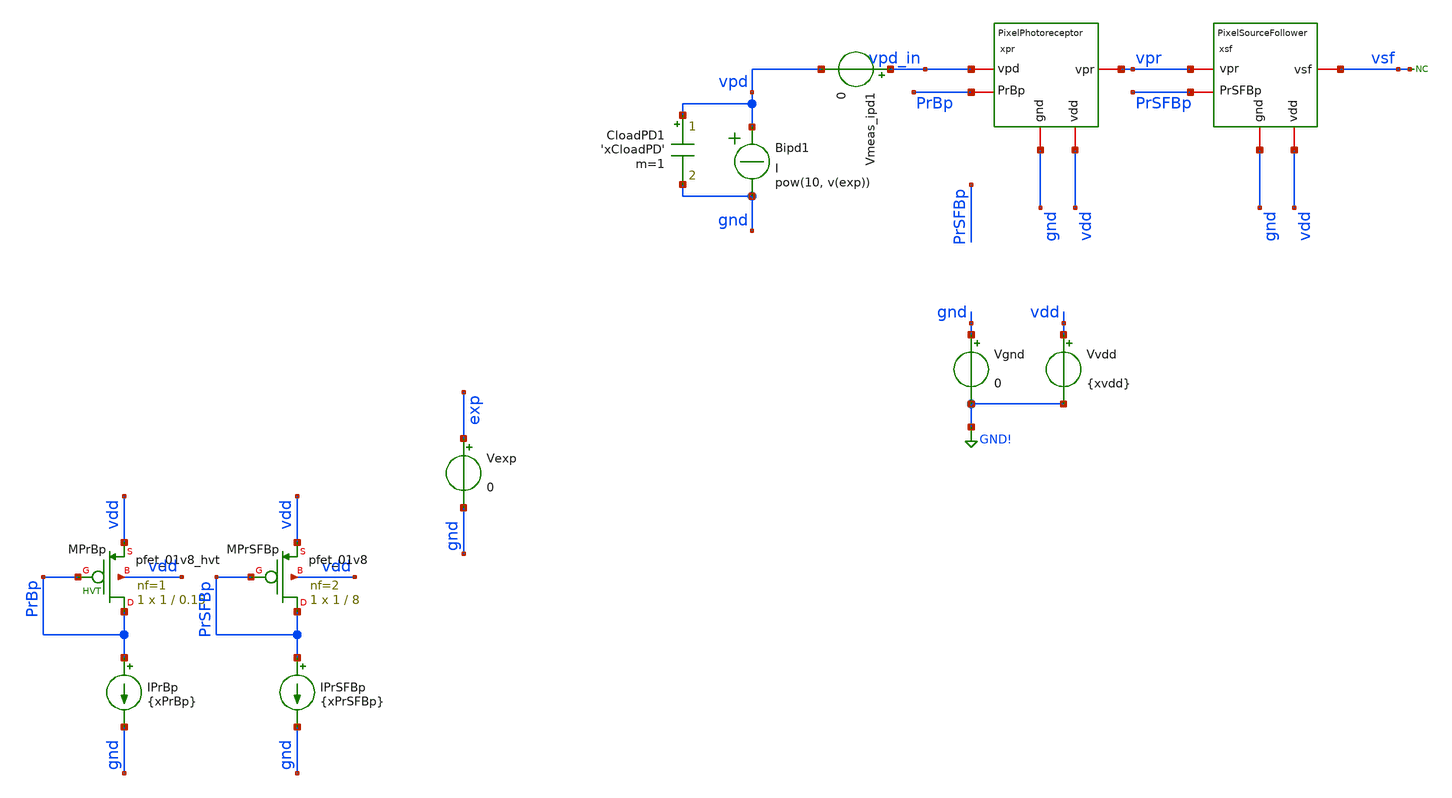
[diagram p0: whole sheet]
** sch_path: analog/klayout/production/final_merge_20260923/testbenches/cace/analog/xschem/tb_PixelPhotoreceptor_dc.sch
**.subckt tb_PixelPhotoreceptor_dc
IPrBp PrBp gnd {xPrBp}
XMPrBp PrBp PrBp vdd vdd sky130_fd_pr__pfet_01v8_hvt L=0.15 W=1 nf=1 ad='int((1 + 1)/2) * 1 / 1 * 0.29'
+ as='int((1 + 2)/2) * 1 / 1 * 0.29' pd='2*int((1 + 1)/2) * (1 / 1 + 0.29)' ps='2*int((1 + 2)/2) * (1 / 1 + 0.29)'
+ nrd='0.29 / 1 ' nrs='0.29 / 1 ' sa=0 sb=0 sd=0 mult=1 m=1
IPrSFBp PrSFBp gnd {xPrSFBp}
XMPrSFBp PrSFBp PrSFBp vdd vdd sky130_fd_pr__pfet_01v8 L=8 W=1 nf=2 ad='int((2 + 1)/2) * 1 / 2 * 0.29'
+ as='int((2 + 2)/2) * 1 / 2 * 0.29' pd='2*int((2 + 1)/2) * (1 / 2 + 0.29)' ps='2*int((2 + 2)/2) * (1 / 2 + 0.29)'
+ nrd='0.29 / 1 ' nrs='0.29 / 1 ' sa=0 sb=0 sd=0 mult=1 m=1
xpr vdd PrBp gnd vpd_in vpr PixelPhotoreceptor
xsf vdd PrSFBp gnd vpr vsf PixelSourceFollower
Bipd1 vpd gnd I = pow(10, v(exp))
CloadPD1 vpd gnd 'xCloadPD' m=1
Vmeas_ipd1 vpd_in vpd 0
* noconn vsf
Vexp exp gnd 0
Vgnd gnd GND! 0
Vvdd vdd GND! {xvdd}
**** begin user architecture code

** opencircuitdesign pdks install
.lib $::SKYWATER_MODELS/sky130.lib.spice tt



.include /home/rpgraca/research/projects/telluride/2025/nic_eventcam/nic2025_openDVS/analog/xschem/dvs_readout_ctrl.spice

** Convergence options for nA-range weak-inversion pixel circuit
** gmin=1e-15: at 1V node this is 1fA shunt, negligible vs nA signals
** method=gear: damps numerical ringing on stiff circuits (fast digital + slow analog)
** trtol=1: conservative timestep control prevents overshoot at edges
.option gmin=1e-16 abstol=1e-15 vntol=1e-9 reltol=1e-4 chgtol=1e-16
.option method=gear maxord=2 trtol=1
.option itl1=500 itl2=200 itl4=50
.option gminsteps=200 srcsteps=200
.option ramptime=100n

.dc Vexp -14 -7 0.2


.param xvdd = 1.8
*.param xipd = 1e-9
.param xPrBp = 10n
.param xPrSFBp = 100p
.param xCloadPD = 30f

** xipd swept via Vexp: Iipd uses behavioral expression

*Small Iphoto testing

.save all



**** end user architecture code
**.ends

* expanding   symbol:  PixelPhotoreceptor.sym # of pins=5
** sym_path: analog/xschem/PixelPhotoreceptor.sym
** sch_path: analog/xschem/PixelPhotoreceptor.sch
.subckt PixelPhotoreceptor vdd PrBp gnd vpd vpr
*.iopin PrBp
*.iopin vdd
*.iopin vpd
*.iopin gnd
*.iopin vpr
XMpd vdd vpr vpd gnd sky130_fd_pr__nfet_01v8 L=0.3 W=0.42 nf=1 ad='int((1 + 1)/2) * 0.42 / 1 * 0.29'
+ as='int((1 + 2)/2) * 0.42 / 1 * 0.29' pd='2*int((1 + 1)/2) * (0.42 / 1 + 0.29)' ps='2*int((1 + 2)/2) * (0.42 / 1 + 0.29)'
+ nrd='0.29 / 0.42 ' nrs='0.29 / 0.42 ' sa=0 sb=0 sd=0 mult=1 m=1
XMpr_amp vpr vpd gnd gnd sky130_fd_pr__nfet_01v8 L=0.3 W=0.42 nf=1 ad='int((1 + 1)/2) * 0.42 / 1 * 0.29'
+ as='int((1 + 2)/2) * 0.42 / 1 * 0.29' pd='2*int((1 + 1)/2) * (0.42 / 1 + 0.29)' ps='2*int((1 + 2)/2) * (0.42 / 1 + 0.29)'
+ nrd='0.29 / 0.42 ' nrs='0.29 / 0.42 ' sa=0 sb=0 sd=0 mult=1 m=1
XMprBias vpr PrBp vdd vdd sky130_fd_pr__pfet_01v8_hvt L=0.15 W=0.5 nf=1 ad='int((1 + 1)/2) * 0.5 / 1 * 0.29'
+ as='int((1 + 2)/2) * 0.5 / 1 * 0.29' pd='2*int((1 + 1)/2) * (0.5 / 1 + 0.29)' ps='2*int((1 + 2)/2) * (0.5 / 1 + 0.29)'
+ nrd='0.29 / 0.5 ' nrs='0.29 / 0.5 ' sa=0 sb=0 sd=0 mult=1 m=1
.ends


* expanding   symbol:  PixelSourceFollower.sym # of pins=5
** sym_path: analog/xschem/PixelSourceFollower.sym
** sch_path: analog/xschem/PixelSourceFollower.sch
.subckt PixelSourceFollower vdd PrSFBp gnd vpr vsf
*.iopin gnd
*.iopin PrSFBp
*.iopin vpr
*.iopin vsf
*.iopin vdd
XMsfBias vsf PrSFBp vdd vdd sky130_fd_pr__pfet_01v8 L=1.6 W=0.42 nf=1 ad='int((1 + 1)/2) * 0.42 / 1 * 0.29'
+ as='int((1 + 2)/2) * 0.42 / 1 * 0.29' pd='2*int((1 + 1)/2) * (0.42 / 1 + 0.29)' ps='2*int((1 + 2)/2) * (0.42 / 1 + 0.29)'
+ nrd='0.29 / 0.42 ' nrs='0.29 / 0.42 ' sa=0 sb=0 sd=0 mult=1 m=1
XMsf gnd vpr vsf vdd sky130_fd_pr__pfet_01v8 L=0.25 W=0.42 nf=1 ad='int((1 + 1)/2) * 0.42 / 1 * 0.29'
+ as='int((1 + 2)/2) * 0.42 / 1 * 0.29' pd='2*int((1 + 1)/2) * (0.42 / 1 + 0.29)' ps='2*int((1 + 2)/2) * (0.42 / 1 + 0.29)'
+ nrd='0.29 / 0.42 ' nrs='0.29 / 0.42 ' sa=0 sb=0 sd=0 mult=1 m=1
.ends

.GLOBAL GND!
.end
